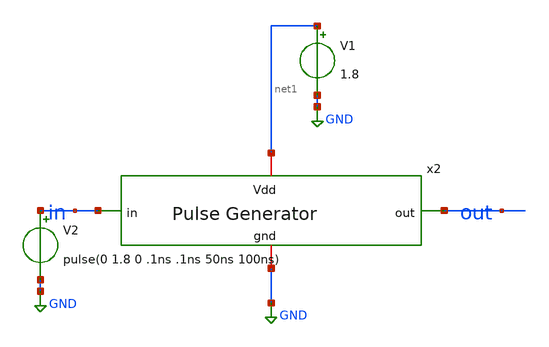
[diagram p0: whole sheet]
** sch_path: xschem/pulse_generator_tb.sch
**.subckt pulse_generator_tb
x1 net1 out in GND pulse_generator
V1 net1 GND 1.8
V2 in GND pulse(0 1.8 0 .1ns .1ns 50ns 100ns)
**** begin user architecture code


.lib /usr/local/share/pdk/sky130A/libs.tech/ngspice/sky130.lib.spice tt

.control
        tran 0.1n 0.2us
	set color0=rgb:f/f/f
	set xbrushwidth=3
        plot v(out) v(in)
.endc
.save all


**** end user architecture code
**.ends

* expanding   symbol:  pulse_generator.sym # of pins=4
** sym_path: xschem/pulse_generator.sym
** sch_path: xschem/pulse_generator.sch
.subckt pulse_generator Vdd out in gnd
*.iopin Vdd
*.ipin in
*.opin out
*.iopin gnd
XM1 net1 in gnd gnd sky130_fd_pr__nfet_01v8 L=0.15 W=1 nf=1 ad='int((nf+1)/2) * W/nf * 0.29' as='int((nf+2)/2) * W/nf * 0.29'
+ pd='2*int((nf+1)/2) * (W/nf + 0.29)' ps='2*int((nf+2)/2) * (W/nf + 0.29)' nrd='0.29 / W' nrs='0.29 / W'
+ sa=0 sb=0 sd=0 mult=1 m=1
XM3 net2 net1 gnd gnd sky130_fd_pr__nfet_01v8 L=0.75 W=1 nf=1 ad='int((nf+1)/2) * W/nf * 0.29' as='int((nf+2)/2) * W/nf * 0.29'
+ pd='2*int((nf+1)/2) * (W/nf + 0.29)' ps='2*int((nf+2)/2) * (W/nf + 0.29)' nrd='0.29 / W' nrs='0.29 / W'
+ sa=0 sb=0 sd=0 mult=1 m=1
XM5 net3 net2 gnd gnd sky130_fd_pr__nfet_01v8 L=0.75 W=1 nf=1 ad='int((nf+1)/2) * W/nf * 0.29' as='int((nf+2)/2) * W/nf * 0.29'
+ pd='2*int((nf+1)/2) * (W/nf + 0.29)' ps='2*int((nf+2)/2) * (W/nf + 0.29)' nrd='0.29 / W' nrs='0.29 / W'
+ sa=0 sb=0 sd=0 mult=1 m=1
XM7 net4 net3 gnd gnd sky130_fd_pr__nfet_01v8 L=0.75 W=1 nf=1 ad='int((nf+1)/2) * W/nf * 0.29' as='int((nf+2)/2) * W/nf * 0.29'
+ pd='2*int((nf+1)/2) * (W/nf + 0.29)' ps='2*int((nf+2)/2) * (W/nf + 0.29)' nrd='0.29 / W' nrs='0.29 / W'
+ sa=0 sb=0 sd=0 mult=1 m=1
XM9 net5 net4 gnd gnd sky130_fd_pr__nfet_01v8 L=0.75 W=1 nf=1 ad='int((nf+1)/2) * W/nf * 0.29' as='int((nf+2)/2) * W/nf * 0.29'
+ pd='2*int((nf+1)/2) * (W/nf + 0.29)' ps='2*int((nf+2)/2) * (W/nf + 0.29)' nrd='0.29 / W' nrs='0.29 / W'
+ sa=0 sb=0 sd=0 mult=1 m=1
XM13 out net5 net6 gnd sky130_fd_pr__nfet_01v8 L=0.75 W=1 nf=1 ad='int((nf+1)/2) * W/nf * 0.29' as='int((nf+2)/2) * W/nf * 0.29'
+ pd='2*int((nf+1)/2) * (W/nf + 0.29)' ps='2*int((nf+2)/2) * (W/nf + 0.29)' nrd='0.29 / W' nrs='0.29 / W'
+ sa=0 sb=0 sd=0 mult=1 m=1
XM14 net6 in gnd gnd sky130_fd_pr__nfet_01v8 L=0.75 W=1 nf=1 ad='int((nf+1)/2) * W/nf * 0.29' as='int((nf+2)/2) * W/nf * 0.29'
+ pd='2*int((nf+1)/2) * (W/nf + 0.29)' ps='2*int((nf+2)/2) * (W/nf + 0.29)' nrd='0.29 / W' nrs='0.29 / W'
+ sa=0 sb=0 sd=0 mult=1 m=1
XM2 net1 in Vdd Vdd sky130_fd_pr__pfet_01v8 L=0.15 W=2 nf=1 ad='int((nf+1)/2) * W/nf * 0.29' as='int((nf+2)/2) * W/nf * 0.29'
+ pd='2*int((nf+1)/2) * (W/nf + 0.29)' ps='2*int((nf+2)/2) * (W/nf + 0.29)' nrd='0.29 / W' nrs='0.29 / W'
+ sa=0 sb=0 sd=0 mult=1 m=1
XM4 net2 net1 Vdd Vdd sky130_fd_pr__pfet_01v8 L=0.75 W=2 nf=1 ad='int((nf+1)/2) * W/nf * 0.29' as='int((nf+2)/2) * W/nf * 0.29'
+ pd='2*int((nf+1)/2) * (W/nf + 0.29)' ps='2*int((nf+2)/2) * (W/nf + 0.29)' nrd='0.29 / W' nrs='0.29 / W'
+ sa=0 sb=0 sd=0 mult=1 m=1
XM6 net3 net2 Vdd Vdd sky130_fd_pr__pfet_01v8 L=0.75 W=2 nf=1 ad='int((nf+1)/2) * W/nf * 0.29' as='int((nf+2)/2) * W/nf * 0.29'
+ pd='2*int((nf+1)/2) * (W/nf + 0.29)' ps='2*int((nf+2)/2) * (W/nf + 0.29)' nrd='0.29 / W' nrs='0.29 / W'
+ sa=0 sb=0 sd=0 mult=1 m=1
XM8 net4 net3 Vdd Vdd sky130_fd_pr__pfet_01v8 L=0.75 W=2 nf=1 ad='int((nf+1)/2) * W/nf * 0.29' as='int((nf+2)/2) * W/nf * 0.29'
+ pd='2*int((nf+1)/2) * (W/nf + 0.29)' ps='2*int((nf+2)/2) * (W/nf + 0.29)' nrd='0.29 / W' nrs='0.29 / W'
+ sa=0 sb=0 sd=0 mult=1 m=1
XM10 net5 net4 Vdd Vdd sky130_fd_pr__pfet_01v8 L=0.75 W=2 nf=1 ad='int((nf+1)/2) * W/nf * 0.29' as='int((nf+2)/2) * W/nf * 0.29'
+ pd='2*int((nf+1)/2) * (W/nf + 0.29)' ps='2*int((nf+2)/2) * (W/nf + 0.29)' nrd='0.29 / W' nrs='0.29 / W'
+ sa=0 sb=0 sd=0 mult=1 m=1
XM11 out net5 Vdd Vdd sky130_fd_pr__pfet_01v8 L=0.75 W=2 nf=1 ad='int((nf+1)/2) * W/nf * 0.29' as='int((nf+2)/2) * W/nf * 0.29'
+ pd='2*int((nf+1)/2) * (W/nf + 0.29)' ps='2*int((nf+2)/2) * (W/nf + 0.29)' nrd='0.29 / W' nrs='0.29 / W'
+ sa=0 sb=0 sd=0 mult=1 m=1
XM12 out in Vdd Vdd sky130_fd_pr__pfet_01v8 L=0.75 W=2 nf=1 ad='int((nf+1)/2) * W/nf * 0.29' as='int((nf+2)/2) * W/nf * 0.29'
+ pd='2*int((nf+1)/2) * (W/nf + 0.29)' ps='2*int((nf+2)/2) * (W/nf + 0.29)' nrd='0.29 / W' nrs='0.29 / W'
+ sa=0 sb=0 sd=0 mult=1 m=1
.ends

.GLOBAL GND
.end
